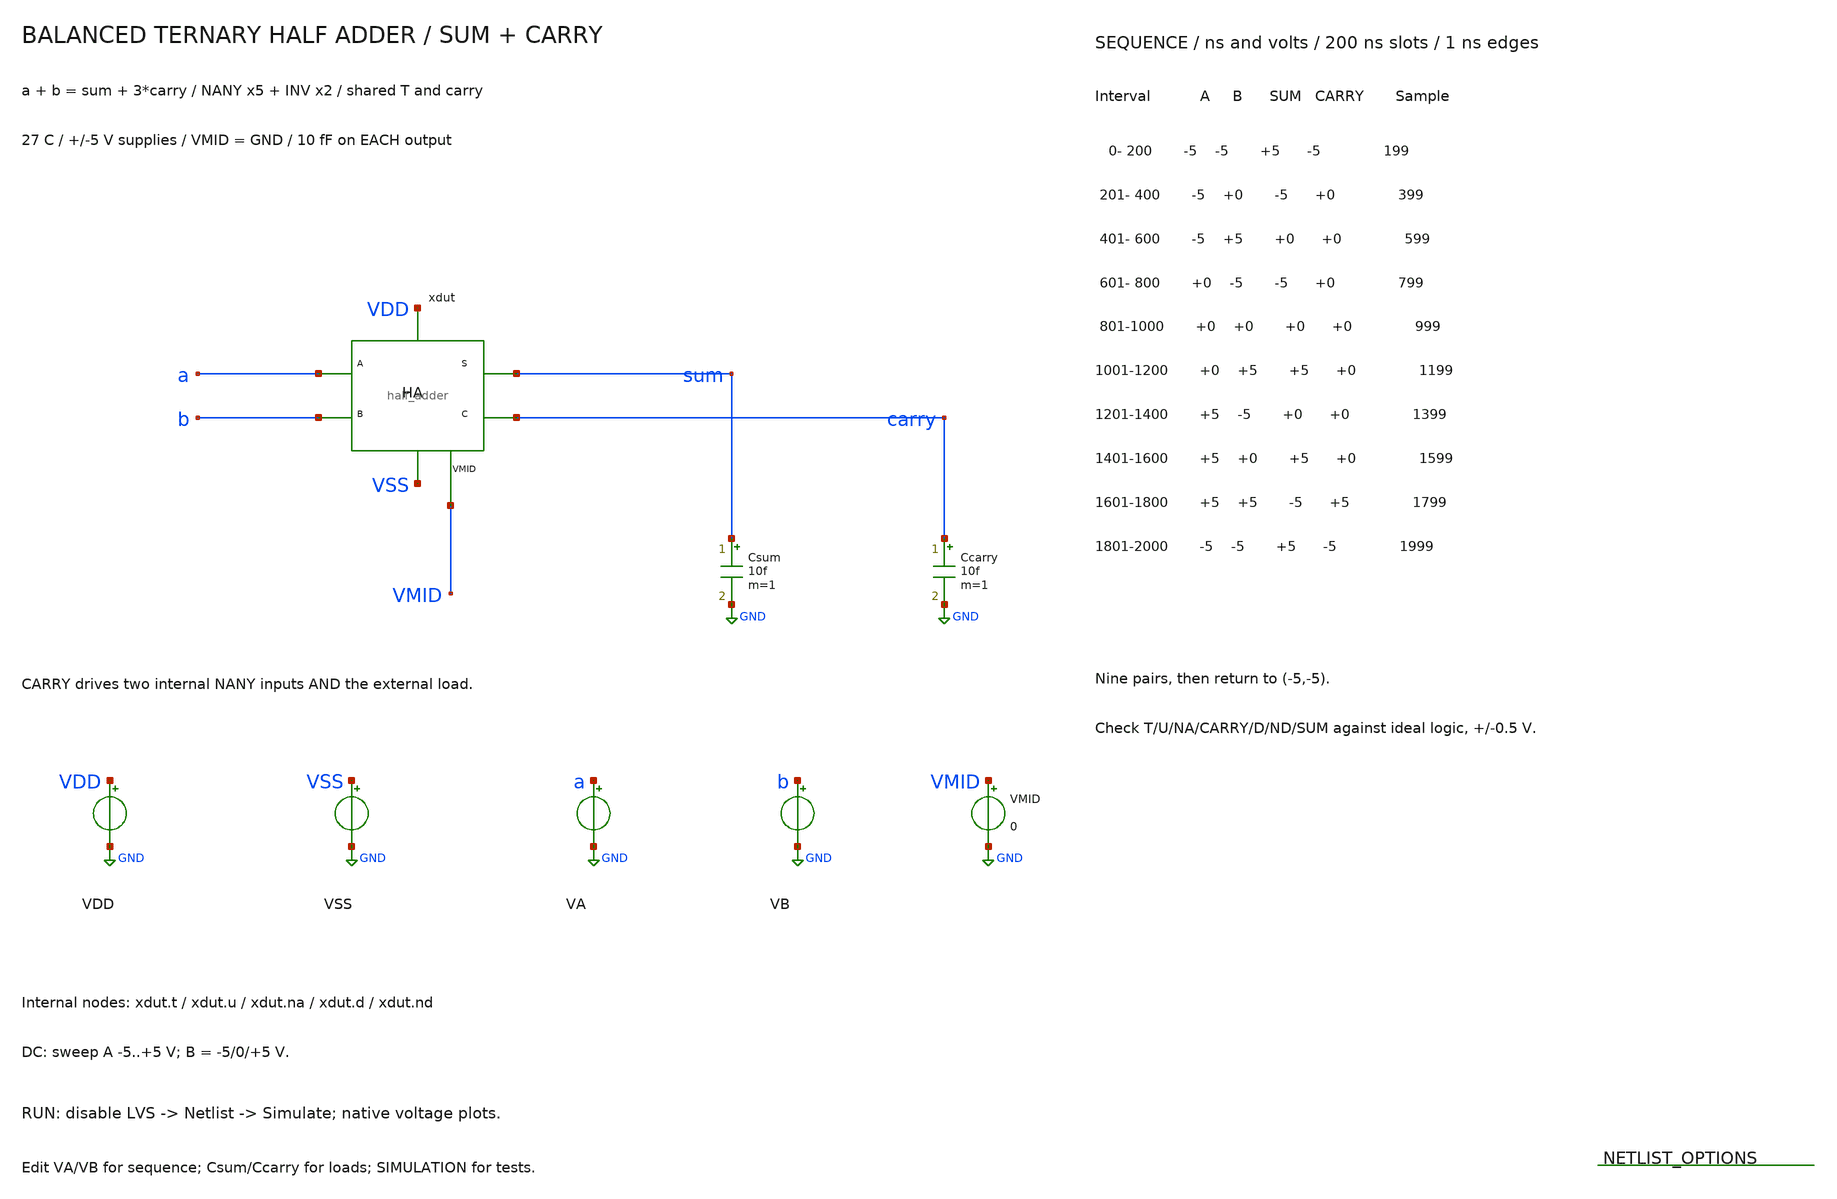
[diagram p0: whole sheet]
** sch_path: member_project/balanced-ternary-logic/PenguinEino/half_adder_tb.sch
**.subckt half_adder_tb
xdut a b sum carry VDD VSS VMID half_adder
Csum sum GND 10f m=1
Ccarry carry GND 10f m=1
VDD VDD GND 5
VSS VSS GND -5
VA a GND PWL(0 -5 200n -5 201n -5 400n -5 401n -5 600n -5 601n 0 800n 0 801n 0 1000n 0 1001n 0 1200n
+ 0 1201n 5 1400n 5 1401n 5 1600n 5 1601n 5 1800n 5 1801n -5 2000n -5)
VB b GND PWL(0 -5 200n -5 201n 0 400n 0 401n 5 600n 5 601n -5 800n -5 801n 0 1000n 0 1001n 5 1200n 5
+ 1201n -5 1400n -5 1401n 0 1600n 0 1601n 5 1800n 5 1801n -5 2000n -5)
VMID VMID GND 0
**** begin user architecture code
 .include $::LIB/ip62_models

.temp 27
.options rshunt=1e12
.param ha_cseed=-5 ha_sseed=5
.nodeset v(xdut.t)=5 v(xdut.u)=0 v(xdut.na)=5 v(carry)={ha_cseed} v(xdut.d)=0 v(xdut.nd)=0 v(sum)={ha_sseed}
.nodeset v(xdut.x_t.net1)=5 v(xdut.x_t.net2)=5 v(xdut.x_t.net3)=-5 v(xdut.x_t.net4)=-5
+ v(xdut.x_t.net5)=0 v(xdut.x_t.net6)=0
.nodeset v(xdut.x_u.net1)=5 v(xdut.x_u.net2)=5 v(xdut.x_u.net3)=-5 v(xdut.x_u.net4)=-5
+ v(xdut.x_u.net5)=0 v(xdut.x_u.net6)=0
.nodeset v(xdut.x_c.net1)=5 v(xdut.x_c.net2)=5 v(xdut.x_c.net3)=-5 v(xdut.x_c.net4)=-5
+ v(xdut.x_c.net5)=0 v(xdut.x_c.net6)=0
.nodeset v(xdut.x_d.net1)=5 v(xdut.x_d.net2)=5 v(xdut.x_d.net3)=-5 v(xdut.x_d.net4)=-5
+ v(xdut.x_d.net5)=0 v(xdut.x_d.net6)=0
.nodeset v(xdut.x_s.net1)=5 v(xdut.x_s.net2)=5 v(xdut.x_s.net3)=-5 v(xdut.x_s.net4)=-5
+ v(xdut.x_s.net5)=0 v(xdut.x_s.net6)=0
.nodeset v(xdut.x_na.net1)=5 v(xdut.x_na.net2)=-5
.nodeset v(xdut.x_nd.net1)=5 v(xdut.x_nd.net2)=-5
.control
save all
set wr_singlescale
set wr_vecnames
setplot const
let failures=0
alterparam ha_cseed=-5
alterparam ha_sseed=5
reset
alter VB -5
dc VA -5 5 0.015625
meas dc dc_0_0_xdut_t find v(xdut.t) at=-5
if abs(dc_0_0_xdut_t-(5)) > 0.5
let const.failures=const.failures+1
echo FAIL: dc_0_0_xdut_t expected 5 V
end
meas dc dc_0_0_xdut_u find v(xdut.u) at=-5
if abs(dc_0_0_xdut_u-(0)) > 0.5
let const.failures=const.failures+1
echo FAIL: dc_0_0_xdut_u expected 0 V
end
meas dc dc_0_0_xdut_na find v(xdut.na) at=-5
if abs(dc_0_0_xdut_na-(5)) > 0.5
let const.failures=const.failures+1
echo FAIL: dc_0_0_xdut_na expected 5 V
end
meas dc dc_0_0_carry find v(carry) at=-5
if abs(dc_0_0_carry-(-5)) > 0.5
let const.failures=const.failures+1
echo FAIL: dc_0_0_carry expected -5 V
end
meas dc dc_0_0_xdut_d find v(xdut.d) at=-5
if abs(dc_0_0_xdut_d-(0)) > 0.5
let const.failures=const.failures+1
echo FAIL: dc_0_0_xdut_d expected 0 V
end
meas dc dc_0_0_xdut_nd find v(xdut.nd) at=-5
if abs(dc_0_0_xdut_nd-(0)) > 0.5
let const.failures=const.failures+1
echo FAIL: dc_0_0_xdut_nd expected 0 V
end
meas dc dc_0_0_sum find v(sum) at=-5
if abs(dc_0_0_sum-(5)) > 0.5
let const.failures=const.failures+1
echo FAIL: dc_0_0_sum expected 5 V
end
meas dc dc_0_1_xdut_t find v(xdut.t) at=0
if abs(dc_0_1_xdut_t-(5)) > 0.5
let const.failures=const.failures+1
echo FAIL: dc_0_1_xdut_t expected 5 V
end
meas dc dc_0_1_xdut_u find v(xdut.u) at=0
if abs(dc_0_1_xdut_u-(0)) > 0.5
let const.failures=const.failures+1
echo FAIL: dc_0_1_xdut_u expected 0 V
end
meas dc dc_0_1_xdut_na find v(xdut.na) at=0
if abs(dc_0_1_xdut_na-(0)) > 0.5
let const.failures=const.failures+1
echo FAIL: dc_0_1_xdut_na expected 0 V
end
meas dc dc_0_1_carry find v(carry) at=0
if abs(dc_0_1_carry-(0)) > 0.5
let const.failures=const.failures+1
echo FAIL: dc_0_1_carry expected 0 V
end
meas dc dc_0_1_xdut_d find v(xdut.d) at=0
if abs(dc_0_1_xdut_d-(-5)) > 0.5
let const.failures=const.failures+1
echo FAIL: dc_0_1_xdut_d expected -5 V
end
meas dc dc_0_1_xdut_nd find v(xdut.nd) at=0
if abs(dc_0_1_xdut_nd-(5)) > 0.5
let const.failures=const.failures+1
echo FAIL: dc_0_1_xdut_nd expected 5 V
end
meas dc dc_0_1_sum find v(sum) at=0
if abs(dc_0_1_sum-(-5)) > 0.5
let const.failures=const.failures+1
echo FAIL: dc_0_1_sum expected -5 V
end
meas dc dc_0_2_xdut_t find v(xdut.t) at=5
if abs(dc_0_2_xdut_t-(0)) > 0.5
let const.failures=const.failures+1
echo FAIL: dc_0_2_xdut_t expected 0 V
end
meas dc dc_0_2_xdut_u find v(xdut.u) at=5
if abs(dc_0_2_xdut_u-(5)) > 0.5
let const.failures=const.failures+1
echo FAIL: dc_0_2_xdut_u expected 5 V
end
meas dc dc_0_2_xdut_na find v(xdut.na) at=5
if abs(dc_0_2_xdut_na-(-5)) > 0.5
let const.failures=const.failures+1
echo FAIL: dc_0_2_xdut_na expected -5 V
end
meas dc dc_0_2_carry find v(carry) at=5
if abs(dc_0_2_carry-(0)) > 0.5
let const.failures=const.failures+1
echo FAIL: dc_0_2_carry expected 0 V
end
meas dc dc_0_2_xdut_d find v(xdut.d) at=5
if abs(dc_0_2_xdut_d-(0)) > 0.5
let const.failures=const.failures+1
echo FAIL: dc_0_2_xdut_d expected 0 V
end
meas dc dc_0_2_xdut_nd find v(xdut.nd) at=5
if abs(dc_0_2_xdut_nd-(0)) > 0.5
let const.failures=const.failures+1
echo FAIL: dc_0_2_xdut_nd expected 0 V
end
meas dc dc_0_2_sum find v(sum) at=5
if abs(dc_0_2_sum-(0)) > 0.5
let const.failures=const.failures+1
echo FAIL: dc_0_2_sum expected 0 V
end
plot v(a) v(sum) v(carry) ylimit -5.5 5.5 title 'Half Adder DC: B=-5 V'
wrdata half_adder_dc_b0.txt v(a) v(b) v(xdut.t) v(xdut.u) v(xdut.na) v(carry) v(xdut.d) v(xdut.nd)
+ v(sum)
alterparam ha_cseed=0
alterparam ha_sseed=0
reset
alter VB 0
dc VA -5 5 0.015625
meas dc dc_1_0_xdut_t find v(xdut.t) at=-5
if abs(dc_1_0_xdut_t-(5)) > 0.5
let const.failures=const.failures+1
echo FAIL: dc_1_0_xdut_t expected 5 V
end
meas dc dc_1_0_xdut_u find v(xdut.u) at=-5
if abs(dc_1_0_xdut_u-(-5)) > 0.5
let const.failures=const.failures+1
echo FAIL: dc_1_0_xdut_u expected -5 V
end
meas dc dc_1_0_xdut_na find v(xdut.na) at=-5
if abs(dc_1_0_xdut_na-(5)) > 0.5
let const.failures=const.failures+1
echo FAIL: dc_1_0_xdut_na expected 5 V
end
meas dc dc_1_0_carry find v(carry) at=-5
if abs(dc_1_0_carry-(0)) > 0.5
let const.failures=const.failures+1
echo FAIL: dc_1_0_carry expected 0 V
end
meas dc dc_1_0_xdut_d find v(xdut.d) at=-5
if abs(dc_1_0_xdut_d-(-5)) > 0.5
let const.failures=const.failures+1
echo FAIL: dc_1_0_xdut_d expected -5 V
end
meas dc dc_1_0_xdut_nd find v(xdut.nd) at=-5
if abs(dc_1_0_xdut_nd-(5)) > 0.5
let const.failures=const.failures+1
echo FAIL: dc_1_0_xdut_nd expected 5 V
end
meas dc dc_1_0_sum find v(sum) at=-5
if abs(dc_1_0_sum-(-5)) > 0.5
let const.failures=const.failures+1
echo FAIL: dc_1_0_sum expected -5 V
end
meas dc dc_1_1_xdut_t find v(xdut.t) at=0
if abs(dc_1_1_xdut_t-(0)) > 0.5
let const.failures=const.failures+1
echo FAIL: dc_1_1_xdut_t expected 0 V
end
meas dc dc_1_1_xdut_u find v(xdut.u) at=0
if abs(dc_1_1_xdut_u-(0)) > 0.5
let const.failures=const.failures+1
echo FAIL: dc_1_1_xdut_u expected 0 V
end
meas dc dc_1_1_xdut_na find v(xdut.na) at=0
if abs(dc_1_1_xdut_na-(0)) > 0.5
let const.failures=const.failures+1
echo FAIL: dc_1_1_xdut_na expected 0 V
end
meas dc dc_1_1_carry find v(carry) at=0
if abs(dc_1_1_carry-(0)) > 0.5
let const.failures=const.failures+1
echo FAIL: dc_1_1_carry expected 0 V
end
meas dc dc_1_1_xdut_d find v(xdut.d) at=0
if abs(dc_1_1_xdut_d-(0)) > 0.5
let const.failures=const.failures+1
echo FAIL: dc_1_1_xdut_d expected 0 V
end
meas dc dc_1_1_xdut_nd find v(xdut.nd) at=0
if abs(dc_1_1_xdut_nd-(0)) > 0.5
let const.failures=const.failures+1
echo FAIL: dc_1_1_xdut_nd expected 0 V
end
meas dc dc_1_1_sum find v(sum) at=0
if abs(dc_1_1_sum-(0)) > 0.5
let const.failures=const.failures+1
echo FAIL: dc_1_1_sum expected 0 V
end
meas dc dc_1_2_xdut_t find v(xdut.t) at=5
if abs(dc_1_2_xdut_t-(-5)) > 0.5
let const.failures=const.failures+1
echo FAIL: dc_1_2_xdut_t expected -5 V
end
meas dc dc_1_2_xdut_u find v(xdut.u) at=5
if abs(dc_1_2_xdut_u-(5)) > 0.5
let const.failures=const.failures+1
echo FAIL: dc_1_2_xdut_u expected 5 V
end
meas dc dc_1_2_xdut_na find v(xdut.na) at=5
if abs(dc_1_2_xdut_na-(-5)) > 0.5
let const.failures=const.failures+1
echo FAIL: dc_1_2_xdut_na expected -5 V
end
meas dc dc_1_2_carry find v(carry) at=5
if abs(dc_1_2_carry-(0)) > 0.5
let const.failures=const.failures+1
echo FAIL: dc_1_2_carry expected 0 V
end
meas dc dc_1_2_xdut_d find v(xdut.d) at=5
if abs(dc_1_2_xdut_d-(5)) > 0.5
let const.failures=const.failures+1
echo FAIL: dc_1_2_xdut_d expected 5 V
end
meas dc dc_1_2_xdut_nd find v(xdut.nd) at=5
if abs(dc_1_2_xdut_nd-(-5)) > 0.5
let const.failures=const.failures+1
echo FAIL: dc_1_2_xdut_nd expected -5 V
end
meas dc dc_1_2_sum find v(sum) at=5
if abs(dc_1_2_sum-(5)) > 0.5
let const.failures=const.failures+1
echo FAIL: dc_1_2_sum expected 5 V
end
plot v(a) v(sum) v(carry) ylimit -5.5 5.5 title 'Half Adder DC: B=0 V'
wrdata half_adder_dc_b1.txt v(a) v(b) v(xdut.t) v(xdut.u) v(xdut.na) v(carry) v(xdut.d) v(xdut.nd)
+ v(sum)
alterparam ha_cseed=-5
alterparam ha_sseed=5
reset
alter VB 5
dc VA -5 5 0.015625
meas dc dc_2_0_xdut_t find v(xdut.t) at=-5
if abs(dc_2_0_xdut_t-(0)) > 0.5
let const.failures=const.failures+1
echo FAIL: dc_2_0_xdut_t expected 0 V
end
meas dc dc_2_0_xdut_u find v(xdut.u) at=-5
if abs(dc_2_0_xdut_u-(-5)) > 0.5
let const.failures=const.failures+1
echo FAIL: dc_2_0_xdut_u expected -5 V
end
meas dc dc_2_0_xdut_na find v(xdut.na) at=-5
if abs(dc_2_0_xdut_na-(5)) > 0.5
let const.failures=const.failures+1
echo FAIL: dc_2_0_xdut_na expected 5 V
end
meas dc dc_2_0_carry find v(carry) at=-5
if abs(dc_2_0_carry-(0)) > 0.5
let const.failures=const.failures+1
echo FAIL: dc_2_0_carry expected 0 V
end
meas dc dc_2_0_xdut_d find v(xdut.d) at=-5
if abs(dc_2_0_xdut_d-(0)) > 0.5
let const.failures=const.failures+1
echo FAIL: dc_2_0_xdut_d expected 0 V
end
meas dc dc_2_0_xdut_nd find v(xdut.nd) at=-5
if abs(dc_2_0_xdut_nd-(0)) > 0.5
let const.failures=const.failures+1
echo FAIL: dc_2_0_xdut_nd expected 0 V
end
meas dc dc_2_0_sum find v(sum) at=-5
if abs(dc_2_0_sum-(0)) > 0.5
let const.failures=const.failures+1
echo FAIL: dc_2_0_sum expected 0 V
end
meas dc dc_2_1_xdut_t find v(xdut.t) at=0
if abs(dc_2_1_xdut_t-(-5)) > 0.5
let const.failures=const.failures+1
echo FAIL: dc_2_1_xdut_t expected -5 V
end
meas dc dc_2_1_xdut_u find v(xdut.u) at=0
if abs(dc_2_1_xdut_u-(0)) > 0.5
let const.failures=const.failures+1
echo FAIL: dc_2_1_xdut_u expected 0 V
end
meas dc dc_2_1_xdut_na find v(xdut.na) at=0
if abs(dc_2_1_xdut_na-(0)) > 0.5
let const.failures=const.failures+1
echo FAIL: dc_2_1_xdut_na expected 0 V
end
meas dc dc_2_1_carry find v(carry) at=0
if abs(dc_2_1_carry-(0)) > 0.5
let const.failures=const.failures+1
echo FAIL: dc_2_1_carry expected 0 V
end
meas dc dc_2_1_xdut_d find v(xdut.d) at=0
if abs(dc_2_1_xdut_d-(5)) > 0.5
let const.failures=const.failures+1
echo FAIL: dc_2_1_xdut_d expected 5 V
end
meas dc dc_2_1_xdut_nd find v(xdut.nd) at=0
if abs(dc_2_1_xdut_nd-(-5)) > 0.5
let const.failures=const.failures+1
echo FAIL: dc_2_1_xdut_nd expected -5 V
end
meas dc dc_2_1_sum find v(sum) at=0
if abs(dc_2_1_sum-(5)) > 0.5
let const.failures=const.failures+1
echo FAIL: dc_2_1_sum expected 5 V
end
meas dc dc_2_2_xdut_t find v(xdut.t) at=5
if abs(dc_2_2_xdut_t-(-5)) > 0.5
let const.failures=const.failures+1
echo FAIL: dc_2_2_xdut_t expected -5 V
end
meas dc dc_2_2_xdut_u find v(xdut.u) at=5
if abs(dc_2_2_xdut_u-(0)) > 0.5
let const.failures=const.failures+1
echo FAIL: dc_2_2_xdut_u expected 0 V
end
meas dc dc_2_2_xdut_na find v(xdut.na) at=5
if abs(dc_2_2_xdut_na-(-5)) > 0.5
let const.failures=const.failures+1
echo FAIL: dc_2_2_xdut_na expected -5 V
end
meas dc dc_2_2_carry find v(carry) at=5
if abs(dc_2_2_carry-(5)) > 0.5
let const.failures=const.failures+1
echo FAIL: dc_2_2_carry expected 5 V
end
meas dc dc_2_2_xdut_d find v(xdut.d) at=5
if abs(dc_2_2_xdut_d-(0)) > 0.5
let const.failures=const.failures+1
echo FAIL: dc_2_2_xdut_d expected 0 V
end
meas dc dc_2_2_xdut_nd find v(xdut.nd) at=5
if abs(dc_2_2_xdut_nd-(0)) > 0.5
let const.failures=const.failures+1
echo FAIL: dc_2_2_xdut_nd expected 0 V
end
meas dc dc_2_2_sum find v(sum) at=5
if abs(dc_2_2_sum-(-5)) > 0.5
let const.failures=const.failures+1
echo FAIL: dc_2_2_sum expected -5 V
end
plot v(a) v(sum) v(carry) ylimit -5.5 5.5 title 'Half Adder DC: B=5 V'
wrdata half_adder_dc_b2.txt v(a) v(b) v(xdut.t) v(xdut.u) v(xdut.na) v(carry) v(xdut.d) v(xdut.nd)
+ v(sum)
alterparam ha_cseed=-5
alterparam ha_sseed=5
reset
tran 0.2n 2000n
let a_logic=5*((v(a)>2.5)-(v(a)<-2.5))
let b_logic=5*((v(b)>2.5)-(v(b)<-2.5))
let carry_expected=5*((v(a)>2.5)*(v(b)>2.5)-(v(a)<-2.5)*(v(b)<-2.5))
let sum_expected=a_logic+b_logic-3*carry_expected
plot v(a) v(b) v(sum) sum_expected title 'Half Adder: SUM'
plot v(a) v(b) v(carry) carry_expected title 'Half Adder: CARRY'
plot v(xdut.t) v(xdut.u) v(xdut.na) v(carry) title 'Half Adder: carry path'
plot v(xdut.d) v(xdut.nd) v(sum) title 'Half Adder: sum path'
wrdata half_adder_tran.txt v(a) v(b) v(xdut.t) v(xdut.u) v(xdut.na) v(carry) v(xdut.d) v(xdut.nd)
+ v(sum)
meas tran tran_0_xdut_t find v(xdut.t) at=199n
if abs(tran_0_xdut_t-(5)) > 0.5
let const.failures=const.failures+1
echo FAIL: tran_0_xdut_t expected 5 V
end
meas tran tran_0_xdut_u find v(xdut.u) at=199n
if abs(tran_0_xdut_u-(0)) > 0.5
let const.failures=const.failures+1
echo FAIL: tran_0_xdut_u expected 0 V
end
meas tran tran_0_xdut_na find v(xdut.na) at=199n
if abs(tran_0_xdut_na-(5)) > 0.5
let const.failures=const.failures+1
echo FAIL: tran_0_xdut_na expected 5 V
end
meas tran tran_0_carry find v(carry) at=199n
if abs(tran_0_carry-(-5)) > 0.5
let const.failures=const.failures+1
echo FAIL: tran_0_carry expected -5 V
end
meas tran tran_0_xdut_d find v(xdut.d) at=199n
if abs(tran_0_xdut_d-(0)) > 0.5
let const.failures=const.failures+1
echo FAIL: tran_0_xdut_d expected 0 V
end
meas tran tran_0_xdut_nd find v(xdut.nd) at=199n
if abs(tran_0_xdut_nd-(0)) > 0.5
let const.failures=const.failures+1
echo FAIL: tran_0_xdut_nd expected 0 V
end
meas tran tran_0_sum find v(sum) at=199n
if abs(tran_0_sum-(5)) > 0.5
let const.failures=const.failures+1
echo FAIL: tran_0_sum expected 5 V
end
meas tran tran_1_xdut_t find v(xdut.t) at=399n
if abs(tran_1_xdut_t-(5)) > 0.5
let const.failures=const.failures+1
echo FAIL: tran_1_xdut_t expected 5 V
end
meas tran tran_1_xdut_u find v(xdut.u) at=399n
if abs(tran_1_xdut_u-(-5)) > 0.5
let const.failures=const.failures+1
echo FAIL: tran_1_xdut_u expected -5 V
end
meas tran tran_1_xdut_na find v(xdut.na) at=399n
if abs(tran_1_xdut_na-(5)) > 0.5
let const.failures=const.failures+1
echo FAIL: tran_1_xdut_na expected 5 V
end
meas tran tran_1_carry find v(carry) at=399n
if abs(tran_1_carry-(0)) > 0.5
let const.failures=const.failures+1
echo FAIL: tran_1_carry expected 0 V
end
meas tran tran_1_xdut_d find v(xdut.d) at=399n
if abs(tran_1_xdut_d-(-5)) > 0.5
let const.failures=const.failures+1
echo FAIL: tran_1_xdut_d expected -5 V
end
meas tran tran_1_xdut_nd find v(xdut.nd) at=399n
if abs(tran_1_xdut_nd-(5)) > 0.5
let const.failures=const.failures+1
echo FAIL: tran_1_xdut_nd expected 5 V
end
meas tran tran_1_sum find v(sum) at=399n
if abs(tran_1_sum-(-5)) > 0.5
let const.failures=const.failures+1
echo FAIL: tran_1_sum expected -5 V
end
meas tran tran_2_xdut_t find v(xdut.t) at=599n
if abs(tran_2_xdut_t-(0)) > 0.5
let const.failures=const.failures+1
echo FAIL: tran_2_xdut_t expected 0 V
end
meas tran tran_2_xdut_u find v(xdut.u) at=599n
if abs(tran_2_xdut_u-(-5)) > 0.5
let const.failures=const.failures+1
echo FAIL: tran_2_xdut_u expected -5 V
end
meas tran tran_2_xdut_na find v(xdut.na) at=599n
if abs(tran_2_xdut_na-(5)) > 0.5
let const.failures=const.failures+1
echo FAIL: tran_2_xdut_na expected 5 V
end
meas tran tran_2_carry find v(carry) at=599n
if abs(tran_2_carry-(0)) > 0.5
let const.failures=const.failures+1
echo FAIL: tran_2_carry expected 0 V
end
meas tran tran_2_xdut_d find v(xdut.d) at=599n
if abs(tran_2_xdut_d-(0)) > 0.5
let const.failures=const.failures+1
echo FAIL: tran_2_xdut_d expected 0 V
end
meas tran tran_2_xdut_nd find v(xdut.nd) at=599n
if abs(tran_2_xdut_nd-(0)) > 0.5
let const.failures=const.failures+1
echo FAIL: tran_2_xdut_nd expected 0 V
end
meas tran tran_2_sum find v(sum) at=599n
if abs(tran_2_sum-(0)) > 0.5
let const.failures=const.failures+1
echo FAIL: tran_2_sum expected 0 V
end
meas tran tran_3_xdut_t find v(xdut.t) at=799n
if abs(tran_3_xdut_t-(5)) > 0.5
let const.failures=const.failures+1
echo FAIL: tran_3_xdut_t expected 5 V
end
meas tran tran_3_xdut_u find v(xdut.u) at=799n
if abs(tran_3_xdut_u-(0)) > 0.5
let const.failures=const.failures+1
echo FAIL: tran_3_xdut_u expected 0 V
end
meas tran tran_3_xdut_na find v(xdut.na) at=799n
if abs(tran_3_xdut_na-(0)) > 0.5
let const.failures=const.failures+1
echo FAIL: tran_3_xdut_na expected 0 V
end
meas tran tran_3_carry find v(carry) at=799n
if abs(tran_3_carry-(0)) > 0.5
let const.failures=const.failures+1
echo FAIL: tran_3_carry expected 0 V
end
meas tran tran_3_xdut_d find v(xdut.d) at=799n
if abs(tran_3_xdut_d-(-5)) > 0.5
let const.failures=const.failures+1
echo FAIL: tran_3_xdut_d expected -5 V
end
meas tran tran_3_xdut_nd find v(xdut.nd) at=799n
if abs(tran_3_xdut_nd-(5)) > 0.5
let const.failures=const.failures+1
echo FAIL: tran_3_xdut_nd expected 5 V
end
meas tran tran_3_sum find v(sum) at=799n
if abs(tran_3_sum-(-5)) > 0.5
let const.failures=const.failures+1
echo FAIL: tran_3_sum expected -5 V
end
meas tran tran_4_xdut_t find v(xdut.t) at=999n
if abs(tran_4_xdut_t-(0)) > 0.5
let const.failures=const.failures+1
echo FAIL: tran_4_xdut_t expected 0 V
end
meas tran tran_4_xdut_u find v(xdut.u) at=999n
if abs(tran_4_xdut_u-(0)) > 0.5
let const.failures=const.failures+1
echo FAIL: tran_4_xdut_u expected 0 V
end
meas tran tran_4_xdut_na find v(xdut.na) at=999n
if abs(tran_4_xdut_na-(0)) > 0.5
let const.failures=const.failures+1
echo FAIL: tran_4_xdut_na expected 0 V
end
meas tran tran_4_carry find v(carry) at=999n
if abs(tran_4_carry-(0)) > 0.5
let const.failures=const.failures+1
echo FAIL: tran_4_carry expected 0 V
end
meas tran tran_4_xdut_d find v(xdut.d) at=999n
if abs(tran_4_xdut_d-(0)) > 0.5
let const.failures=const.failures+1
echo FAIL: tran_4_xdut_d expected 0 V
end
meas tran tran_4_xdut_nd find v(xdut.nd) at=999n
if abs(tran_4_xdut_nd-(0)) > 0.5
let const.failures=const.failures+1
echo FAIL: tran_4_xdut_nd expected 0 V
end
meas tran tran_4_sum find v(sum) at=999n
if abs(tran_4_sum-(0)) > 0.5
let const.failures=const.failures+1
echo FAIL: tran_4_sum expected 0 V
end
meas tran tran_5_xdut_t find v(xdut.t) at=1199n
if abs(tran_5_xdut_t-(-5)) > 0.5
let const.failures=const.failures+1
echo FAIL: tran_5_xdut_t expected -5 V
end
meas tran tran_5_xdut_u find v(xdut.u) at=1199n
if abs(tran_5_xdut_u-(0)) > 0.5
let const.failures=const.failures+1
echo FAIL: tran_5_xdut_u expected 0 V
end
meas tran tran_5_xdut_na find v(xdut.na) at=1199n
if abs(tran_5_xdut_na-(0)) > 0.5
let const.failures=const.failures+1
echo FAIL: tran_5_xdut_na expected 0 V
end
meas tran tran_5_carry find v(carry) at=1199n
if abs(tran_5_carry-(0)) > 0.5
let const.failures=const.failures+1
echo FAIL: tran_5_carry expected 0 V
end
meas tran tran_5_xdut_d find v(xdut.d) at=1199n
if abs(tran_5_xdut_d-(5)) > 0.5
let const.failures=const.failures+1
echo FAIL: tran_5_xdut_d expected 5 V
end
meas tran tran_5_xdut_nd find v(xdut.nd) at=1199n
if abs(tran_5_xdut_nd-(-5)) > 0.5
let const.failures=const.failures+1
echo FAIL: tran_5_xdut_nd expected -5 V
end
meas tran tran_5_sum find v(sum) at=1199n
if abs(tran_5_sum-(5)) > 0.5
let const.failures=const.failures+1
echo FAIL: tran_5_sum expected 5 V
end
meas tran tran_6_xdut_t find v(xdut.t) at=1399n
if abs(tran_6_xdut_t-(0)) > 0.5
let const.failures=const.failures+1
echo FAIL: tran_6_xdut_t expected 0 V
end
meas tran tran_6_xdut_u find v(xdut.u) at=1399n
if abs(tran_6_xdut_u-(5)) > 0.5
let const.failures=const.failures+1
echo FAIL: tran_6_xdut_u expected 5 V
end
meas tran tran_6_xdut_na find v(xdut.na) at=1399n
if abs(tran_6_xdut_na-(-5)) > 0.5
let const.failures=const.failures+1
echo FAIL: tran_6_xdut_na expected -5 V
end
meas tran tran_6_carry find v(carry) at=1399n
if abs(tran_6_carry-(0)) > 0.5
let const.failures=const.failures+1
echo FAIL: tran_6_carry expected 0 V
end
meas tran tran_6_xdut_d find v(xdut.d) at=1399n
if abs(tran_6_xdut_d-(0)) > 0.5
let const.failures=const.failures+1
echo FAIL: tran_6_xdut_d expected 0 V
end
meas tran tran_6_xdut_nd find v(xdut.nd) at=1399n
if abs(tran_6_xdut_nd-(0)) > 0.5
let const.failures=const.failures+1
echo FAIL: tran_6_xdut_nd expected 0 V
end
meas tran tran_6_sum find v(sum) at=1399n
if abs(tran_6_sum-(0)) > 0.5
let const.failures=const.failures+1
echo FAIL: tran_6_sum expected 0 V
end
meas tran tran_7_xdut_t find v(xdut.t) at=1599n
if abs(tran_7_xdut_t-(-5)) > 0.5
let const.failures=const.failures+1
echo FAIL: tran_7_xdut_t expected -5 V
end
meas tran tran_7_xdut_u find v(xdut.u) at=1599n
if abs(tran_7_xdut_u-(5)) > 0.5
let const.failures=const.failures+1
echo FAIL: tran_7_xdut_u expected 5 V
end
meas tran tran_7_xdut_na find v(xdut.na) at=1599n
if abs(tran_7_xdut_na-(-5)) > 0.5
let const.failures=const.failures+1
echo FAIL: tran_7_xdut_na expected -5 V
end
meas tran tran_7_carry find v(carry) at=1599n
if abs(tran_7_carry-(0)) > 0.5
let const.failures=const.failures+1
echo FAIL: tran_7_carry expected 0 V
end
meas tran tran_7_xdut_d find v(xdut.d) at=1599n
if abs(tran_7_xdut_d-(5)) > 0.5
let const.failures=const.failures+1
echo FAIL: tran_7_xdut_d expected 5 V
end
meas tran tran_7_xdut_nd find v(xdut.nd) at=1599n
if abs(tran_7_xdut_nd-(-5)) > 0.5
let const.failures=const.failures+1
echo FAIL: tran_7_xdut_nd expected -5 V
end
meas tran tran_7_sum find v(sum) at=1599n
if abs(tran_7_sum-(5)) > 0.5
let const.failures=const.failures+1
echo FAIL: tran_7_sum expected 5 V
end
meas tran tran_8_xdut_t find v(xdut.t) at=1799n
if abs(tran_8_xdut_t-(-5)) > 0.5
let const.failures=const.failures+1
echo FAIL: tran_8_xdut_t expected -5 V
end
meas tran tran_8_xdut_u find v(xdut.u) at=1799n
if abs(tran_8_xdut_u-(0)) > 0.5
let const.failures=const.failures+1
echo FAIL: tran_8_xdut_u expected 0 V
end
meas tran tran_8_xdut_na find v(xdut.na) at=1799n
if abs(tran_8_xdut_na-(-5)) > 0.5
let const.failures=const.failures+1
echo FAIL: tran_8_xdut_na expected -5 V
end
meas tran tran_8_carry find v(carry) at=1799n
if abs(tran_8_carry-(5)) > 0.5
let const.failures=const.failures+1
echo FAIL: tran_8_carry expected 5 V
end
meas tran tran_8_xdut_d find v(xdut.d) at=1799n
if abs(tran_8_xdut_d-(0)) > 0.5
let const.failures=const.failures+1
echo FAIL: tran_8_xdut_d expected 0 V
end
meas tran tran_8_xdut_nd find v(xdut.nd) at=1799n
if abs(tran_8_xdut_nd-(0)) > 0.5
let const.failures=const.failures+1
echo FAIL: tran_8_xdut_nd expected 0 V
end
meas tran tran_8_sum find v(sum) at=1799n
if abs(tran_8_sum-(-5)) > 0.5
let const.failures=const.failures+1
echo FAIL: tran_8_sum expected -5 V
end
meas tran tran_9_xdut_t find v(xdut.t) at=1999n
if abs(tran_9_xdut_t-(5)) > 0.5
let const.failures=const.failures+1
echo FAIL: tran_9_xdut_t expected 5 V
end
meas tran tran_9_xdut_u find v(xdut.u) at=1999n
if abs(tran_9_xdut_u-(0)) > 0.5
let const.failures=const.failures+1
echo FAIL: tran_9_xdut_u expected 0 V
end
meas tran tran_9_xdut_na find v(xdut.na) at=1999n
if abs(tran_9_xdut_na-(5)) > 0.5
let const.failures=const.failures+1
echo FAIL: tran_9_xdut_na expected 5 V
end
meas tran tran_9_carry find v(carry) at=1999n
if abs(tran_9_carry-(-5)) > 0.5
let const.failures=const.failures+1
echo FAIL: tran_9_carry expected -5 V
end
meas tran tran_9_xdut_d find v(xdut.d) at=1999n
if abs(tran_9_xdut_d-(0)) > 0.5
let const.failures=const.failures+1
echo FAIL: tran_9_xdut_d expected 0 V
end
meas tran tran_9_xdut_nd find v(xdut.nd) at=1999n
if abs(tran_9_xdut_nd-(0)) > 0.5
let const.failures=const.failures+1
echo FAIL: tran_9_xdut_nd expected 0 V
end
meas tran tran_9_sum find v(sum) at=1999n
if abs(tran_9_sum-(5)) > 0.5
let const.failures=const.failures+1
echo FAIL: tran_9_sum expected 5 V
end
if const.failures = 0
echo PASS: Half Adder DC/transient outputs and internal nodes
else
echo FAIL: Half Adder samples outside +/-0.5 V
end
print const.failures
.endc

**** end user architecture code
**.ends

* expanding   symbol:  /home/ishi-kai/balanced-ternary-logic/half_adder.sym # of pins=7
** sym_path: member_project/balanced-ternary-logic/PenguinEino/half_adder.sym
** sch_path: member_project/balanced-ternary-logic/PenguinEino/half_adder.sch
.subckt half_adder a b sum carry VDD VSS VMID
*.ipin a
*.ipin b
*.opin carry
*.iopin VDD
*.iopin VSS
*.iopin VMID
*.opin sum
x_t a b t VDD VSS VMID nany
x_u b t u VDD VSS VMID nany
x_na a na VDD VSS inverter
x_c na u carry VDD VSS VMID nany
x_d t carry d VDD VSS VMID nany
x_nd d nd VDD VSS inverter
x_s nd carry sum VDD VSS VMID nany
.ends


* expanding   symbol:  /home/ishi-kai/balanced-ternary-logic/nany.sym # of pins=6
** sym_path: member_project/balanced-ternary-logic/PenguinEino/submission/nany.sym
** sch_path: member_project/balanced-ternary-logic/PenguinEino/submission/nany.sch
.subckt nany a b vout VDD VSS VMID
*.iopin VDD
*.ipin a
*.ipin b
*.opin vout
*.iopin VSS
*.iopin VMID
XXM3 net2 b net1 VDD PMOS w=34u l=1u nrd=0 nrs=0 m=1
XR2 net2 vout VDD F_RR w=2.8e-06 l=30e-06 R=1 tc1=0 tc2=0 m=1
XR1 vout net3 VDD F_RR w=2.8e-06 l=30e-06 R=1 tc1=0 tc2=0 m=1
XXM2 net3 a net4 VSS NMOS w=11u l=1u nrd=0 nrs=0 m=1
XXM1 net4 b VSS VSS NMOS w=11u l=1u nrd=0 nrs=0 m=1
XXM5 net1 a VDD VDD PMOS w=34u l=1u nrd=0 nrs=0 m=1
XXM6 net5 a vout VDD PMOS w=14u l=1u nrd=0 nrs=0 m=1
XXM7 net5 b VMID VSS NMOS w=8u l=1u nrd=0 nrs=0 m=1
XXM8 net6 b vout VDD PMOS w=14u l=1u nrd=0 nrs=0 m=1
XXM9 net6 a VMID VSS NMOS w=8u l=1u nrd=0 nrs=0 m=1
.ends


* expanding   symbol:  /home/ishi-kai/balanced-ternary-logic/inverter.sym # of pins=4
** sym_path: member_project/balanced-ternary-logic/PenguinEino/inverter.sym
** sch_path: member_project/balanced-ternary-logic/PenguinEino/inverter.sch
.subckt inverter vin vout VDD VSS
*.iopin VDD
*.ipin vin
*.opin vout
*.iopin VSS
XXM1 net1 vin VDD VDD PMOS w=13.5u l=1u nrd=0 nrs=0 m=1
XR1 net1 vout VDD F_RR w=2.8e-06 l=30e-06 R=1 tc1=0 tc2=0 m=1
XR2 vout net2 VDD F_RR w=2.8e-06 l=30e-06 R=1 tc1=0 tc2=0 m=1
XXM2 net2 vin VSS VSS NMOS w=5u l=1u nrd=0 nrs=0 m=1
.ends

.GLOBAL GND
.end
